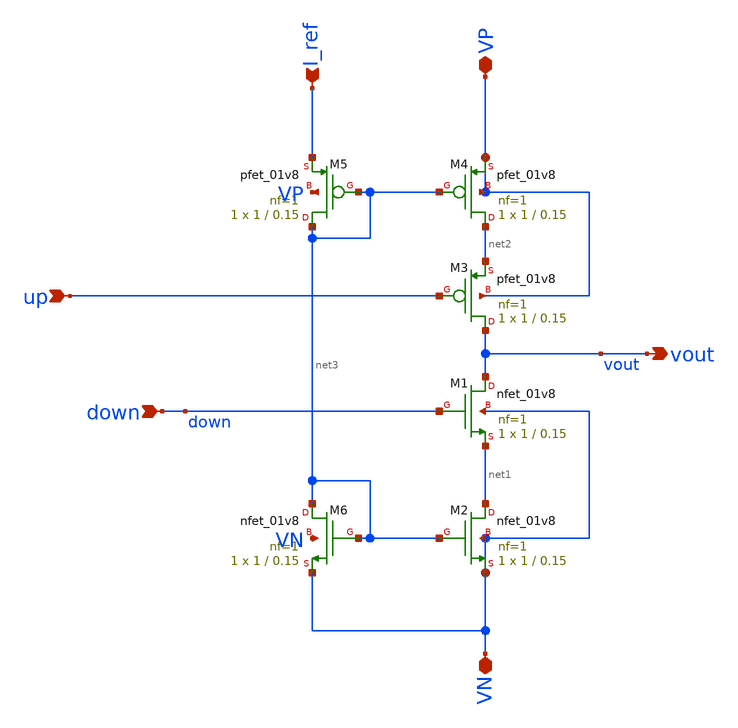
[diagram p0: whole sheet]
** sch_path: git_11/CHRG_PUMP.sch
**.subckt CHRG_PUMP I_ref up down VN VP vout
*.ipin I_ref
*.ipin up
*.ipin down
*.iopin VN
*.iopin VP
*.opin vout
XM1 vout down net1 VN sky130_fd_pr__nfet_01v8 L=0.15 W=1 nf=1 ad='int((nf+1)/2) * W/nf * 0.29' as='int((nf+2)/2) * W/nf * 0.29'
+ pd='2*int((nf+1)/2) * (W/nf + 0.29)' ps='2*int((nf+2)/2) * (W/nf + 0.29)' nrd='0.29 / W' nrs='0.29 / W'
+ sa=0 sb=0 sd=0 mult=1 m=1
XM2 net1 net3 VN VN sky130_fd_pr__nfet_01v8 L=0.15 W=1 nf=1 ad='int((nf+1)/2) * W/nf * 0.29' as='int((nf+2)/2) * W/nf * 0.29'
+ pd='2*int((nf+1)/2) * (W/nf + 0.29)' ps='2*int((nf+2)/2) * (W/nf + 0.29)' nrd='0.29 / W' nrs='0.29 / W'
+ sa=0 sb=0 sd=0 mult=1 m=1
XM3 vout up net2 VP sky130_fd_pr__pfet_01v8 L=0.15 W=1 nf=1 ad='int((nf+1)/2) * W/nf * 0.29' as='int((nf+2)/2) * W/nf * 0.29'
+ pd='2*int((nf+1)/2) * (W/nf + 0.29)' ps='2*int((nf+2)/2) * (W/nf + 0.29)' nrd='0.29 / W' nrs='0.29 / W'
+ sa=0 sb=0 sd=0 mult=1 m=1
XM4 net2 net3 VP VP sky130_fd_pr__pfet_01v8 L=0.15 W=1 nf=1 ad='int((nf+1)/2) * W/nf * 0.29' as='int((nf+2)/2) * W/nf * 0.29'
+ pd='2*int((nf+1)/2) * (W/nf + 0.29)' ps='2*int((nf+2)/2) * (W/nf + 0.29)' nrd='0.29 / W' nrs='0.29 / W'
+ sa=0 sb=0 sd=0 mult=1 m=1
XM5 net3 net3 I_ref VP sky130_fd_pr__pfet_01v8 L=0.15 W=1 nf=1 ad='int((nf+1)/2) * W/nf * 0.29' as='int((nf+2)/2) * W/nf * 0.29'
+ pd='2*int((nf+1)/2) * (W/nf + 0.29)' ps='2*int((nf+2)/2) * (W/nf + 0.29)' nrd='0.29 / W' nrs='0.29 / W'
+ sa=0 sb=0 sd=0 mult=1 m=1
XM6 net3 net3 VN VN sky130_fd_pr__nfet_01v8 L=0.15 W=1 nf=1 ad='int((nf+1)/2) * W/nf * 0.29' as='int((nf+2)/2) * W/nf * 0.29'
+ pd='2*int((nf+1)/2) * (W/nf + 0.29)' ps='2*int((nf+2)/2) * (W/nf + 0.29)' nrd='0.29 / W' nrs='0.29 / W'
+ sa=0 sb=0 sd=0 mult=1 m=1
**.ends
.end
